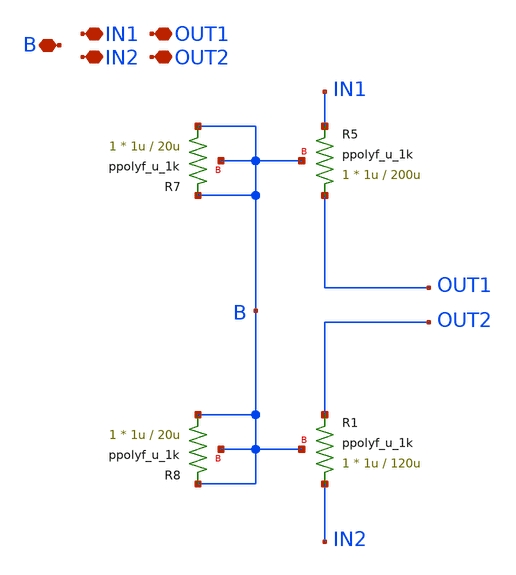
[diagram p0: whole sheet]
** sch_path: LDO/xschem/resistor/symbol/resistor.sch
**.subckt resistor OUT1 IN2 IN1 B OUT2
*.iopin OUT1
*.iopin IN2
*.iopin IN1
*.iopin B
*.iopin OUT2
XR5 OUT1 IN1 B ppolyf_u_1k r_width=1u r_length=200u m=1
XR7 B B B ppolyf_u_1k r_width=1u r_length=20u m=1
XR8 B B B ppolyf_u_1k r_width=1u r_length=20u m=1
XR1 IN2 OUT2 B ppolyf_u_1k r_width=1u r_length=120u m=1
**.ends
.end
